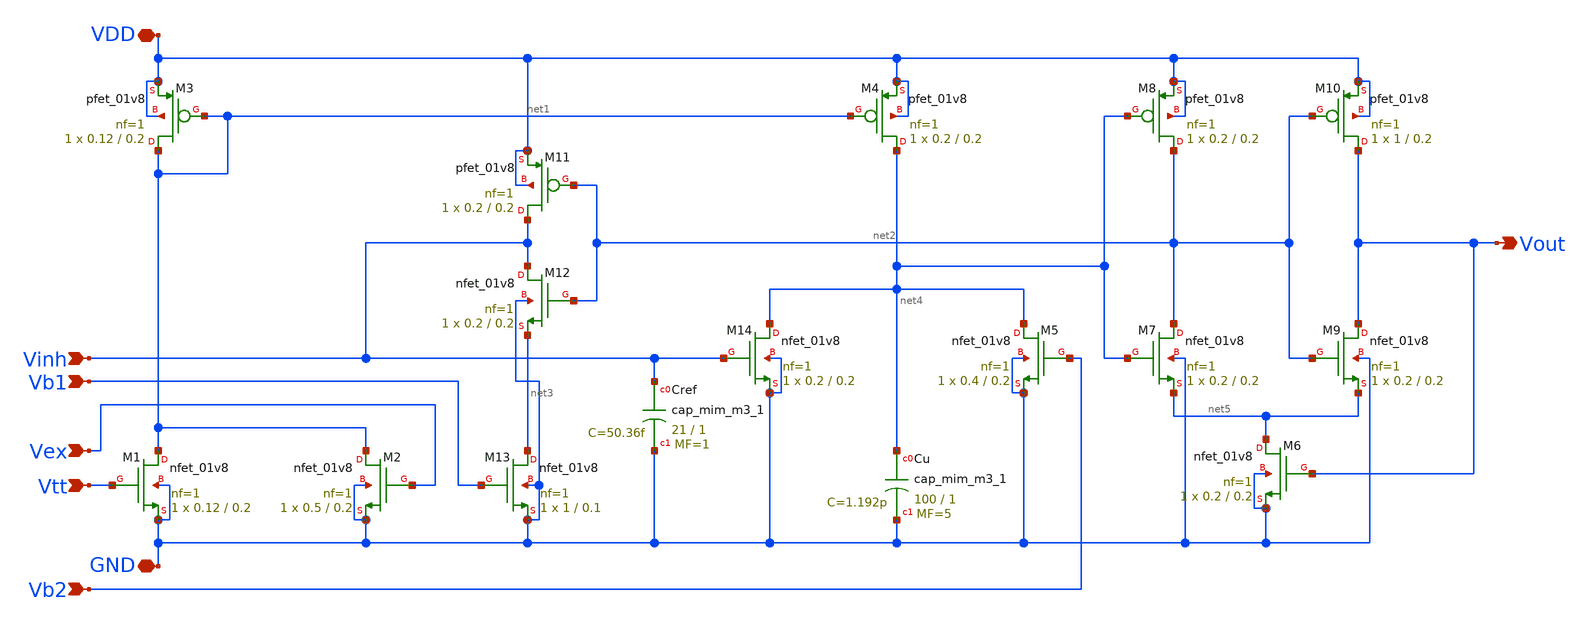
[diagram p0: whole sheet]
** sch_path: LIF_neuron/LIF_neuron_Shamsi.sch
**.subckt LIF_neuron_Shamsi Vtt Vex GND Vinh Vb1 Vb2 VDD Vout
*.ipin Vtt
*.ipin Vex
*.iopin GND
*.ipin Vinh
*.ipin Vb1
*.ipin Vb2
*.iopin VDD
*.opin Vout
XM1 net1 Vtt GND GND sky130_fd_pr__nfet_01v8 L=0.2 W=0.12 nf=1 ad='int((nf+1)/2) * W/nf * 0.29' as='int((nf+2)/2) * W/nf * 0.29'
+ pd='2*int((nf+1)/2) * (W/nf + 0.29)' ps='2*int((nf+2)/2) * (W/nf + 0.29)' nrd='0.29 / W' nrs='0.29 / W'
+ sa=0 sb=0 sd=0 mult=1 m=1
XM3 net1 net1 VDD VDD sky130_fd_pr__pfet_01v8 L=0.2 W=0.12 nf=1 ad='int((nf+1)/2) * W/nf * 0.29' as='int((nf+2)/2) * W/nf * 0.29'
+ pd='2*int((nf+1)/2) * (W/nf + 0.29)' ps='2*int((nf+2)/2) * (W/nf + 0.29)' nrd='0.29 / W' nrs='0.29 / W'
+ sa=0 sb=0 sd=0 mult=1 m=1
XM2 net1 Vex GND GND sky130_fd_pr__nfet_01v8 L=0.2 W=0.5 nf=1 ad='int((nf+1)/2) * W/nf * 0.29' as='int((nf+2)/2) * W/nf * 0.29'
+ pd='2*int((nf+1)/2) * (W/nf + 0.29)' ps='2*int((nf+2)/2) * (W/nf + 0.29)' nrd='0.29 / W' nrs='0.29 / W'
+ sa=0 sb=0 sd=0 mult=1 m=1
XM13 net3 Vb1 GND GND sky130_fd_pr__nfet_01v8 L=0.1 W=1 nf=1 ad='int((nf+1)/2) * W/nf * 0.29' as='int((nf+2)/2) * W/nf * 0.29'
+ pd='2*int((nf+1)/2) * (W/nf + 0.29)' ps='2*int((nf+2)/2) * (W/nf + 0.29)' nrd='0.29 / W' nrs='0.29 / W'
+ sa=0 sb=0 sd=0 mult=1 m=1
XM12 Vinh net2 net3 GND sky130_fd_pr__nfet_01v8 L=0.2 W=0.2 nf=1 ad='int((nf+1)/2) * W/nf * 0.29' as='int((nf+2)/2) * W/nf * 0.29'
+ pd='2*int((nf+1)/2) * (W/nf + 0.29)' ps='2*int((nf+2)/2) * (W/nf + 0.29)' nrd='0.29 / W' nrs='0.29 / W'
+ sa=0 sb=0 sd=0 mult=1 m=1
XM11 Vinh net2 VDD VDD sky130_fd_pr__pfet_01v8 L=0.2 W=0.2 nf=1 ad='int((nf+1)/2) * W/nf * 0.29' as='int((nf+2)/2) * W/nf * 0.29'
+ pd='2*int((nf+1)/2) * (W/nf + 0.29)' ps='2*int((nf+2)/2) * (W/nf + 0.29)' nrd='0.29 / W' nrs='0.29 / W'
+ sa=0 sb=0 sd=0 mult=1 m=1
XCref Vinh GND sky130_fd_pr__cap_mim_m3_1 W=21 L=1 MF=1 m=1
XM14 net4 Vinh GND GND sky130_fd_pr__nfet_01v8 L=0.2 W=0.2 nf=1 ad='int((nf+1)/2) * W/nf * 0.29' as='int((nf+2)/2) * W/nf * 0.29'
+ pd='2*int((nf+1)/2) * (W/nf + 0.29)' ps='2*int((nf+2)/2) * (W/nf + 0.29)' nrd='0.29 / W' nrs='0.29 / W'
+ sa=0 sb=0 sd=0 mult=1 m=1
XM4 net4 net1 VDD VDD sky130_fd_pr__pfet_01v8 L=0.2 W=0.2 nf=1 ad='int((nf+1)/2) * W/nf * 0.29' as='int((nf+2)/2) * W/nf * 0.29'
+ pd='2*int((nf+1)/2) * (W/nf + 0.29)' ps='2*int((nf+2)/2) * (W/nf + 0.29)' nrd='0.29 / W' nrs='0.29 / W'
+ sa=0 sb=0 sd=0 mult=1 m=1
XCu net4 GND sky130_fd_pr__cap_mim_m3_1 W=100 L=1 MF=5 m=5
XM5 net4 Vb2 GND GND sky130_fd_pr__nfet_01v8 L=0.2 W=0.4 nf=1 ad='int((nf+1)/2) * W/nf * 0.29' as='int((nf+2)/2) * W/nf * 0.29'
+ pd='2*int((nf+1)/2) * (W/nf + 0.29)' ps='2*int((nf+2)/2) * (W/nf + 0.29)' nrd='0.29 / W' nrs='0.29 / W'
+ sa=0 sb=0 sd=0 mult=1 m=1
XM6 net5 Vout GND GND sky130_fd_pr__nfet_01v8 L=0.2 W=0.2 nf=1 ad='int((nf+1)/2) * W/nf * 0.29' as='int((nf+2)/2) * W/nf * 0.29'
+ pd='2*int((nf+1)/2) * (W/nf + 0.29)' ps='2*int((nf+2)/2) * (W/nf + 0.29)' nrd='0.29 / W' nrs='0.29 / W'
+ sa=0 sb=0 sd=0 mult=1 m=1
XM7 net2 net4 net5 GND sky130_fd_pr__nfet_01v8 L=0.2 W=0.2 nf=1 ad='int((nf+1)/2) * W/nf * 0.29' as='int((nf+2)/2) * W/nf * 0.29'
+ pd='2*int((nf+1)/2) * (W/nf + 0.29)' ps='2*int((nf+2)/2) * (W/nf + 0.29)' nrd='0.29 / W' nrs='0.29 / W'
+ sa=0 sb=0 sd=0 mult=1 m=1
XM8 net2 net4 VDD VDD sky130_fd_pr__pfet_01v8 L=0.2 W=0.2 nf=1 ad='int((nf+1)/2) * W/nf * 0.29' as='int((nf+2)/2) * W/nf * 0.29'
+ pd='2*int((nf+1)/2) * (W/nf + 0.29)' ps='2*int((nf+2)/2) * (W/nf + 0.29)' nrd='0.29 / W' nrs='0.29 / W'
+ sa=0 sb=0 sd=0 mult=1 m=1
XM9 Vout net2 net5 GND sky130_fd_pr__nfet_01v8 L=0.2 W=0.2 nf=1 ad='int((nf+1)/2) * W/nf * 0.29' as='int((nf+2)/2) * W/nf * 0.29'
+ pd='2*int((nf+1)/2) * (W/nf + 0.29)' ps='2*int((nf+2)/2) * (W/nf + 0.29)' nrd='0.29 / W' nrs='0.29 / W'
+ sa=0 sb=0 sd=0 mult=1 m=1
XM10 Vout net2 VDD VDD sky130_fd_pr__pfet_01v8 L=0.2 W=1 nf=1 ad='int((nf+1)/2) * W/nf * 0.29' as='int((nf+2)/2) * W/nf * 0.29'
+ pd='2*int((nf+1)/2) * (W/nf + 0.29)' ps='2*int((nf+2)/2) * (W/nf + 0.29)' nrd='0.29 / W' nrs='0.29 / W'
+ sa=0 sb=0 sd=0 mult=1 m=1
**.ends
.end
